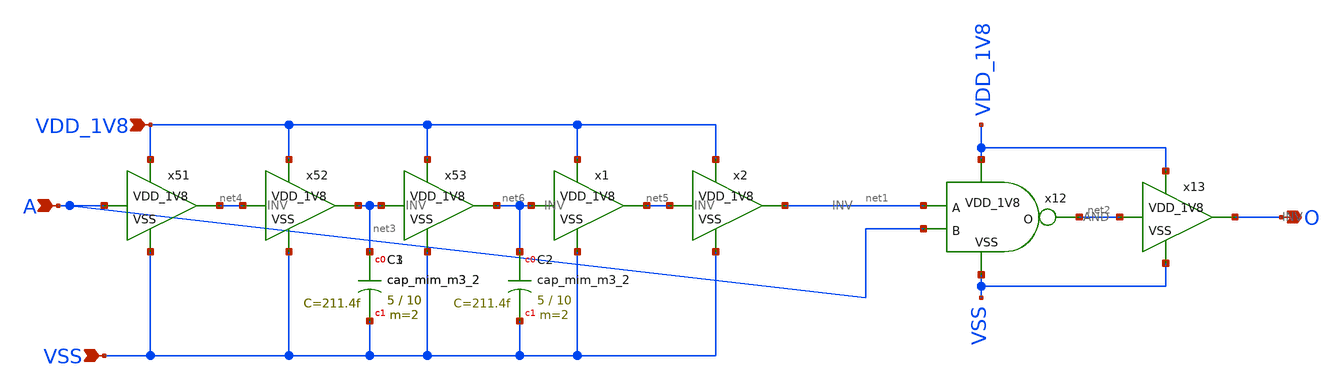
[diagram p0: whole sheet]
** sch_path: design/CNR_GR05_SKY130NM/POSEDGE.sch
**.subckt POSEDGE O VDD_1V8 VSS A
*.opin O
*.ipin VDD_1V8
*.ipin VSS
*.ipin A
x12 VDD_1V8 net1 A net2 VSS AND
x13 VDD_1V8 net2 O VSS INV
x51 VDD_1V8 A net4 VSS INV
x52 VDD_1V8 net4 net3 VSS INV
x53 VDD_1V8 net3 net6 VSS INV
x1 VDD_1V8 net6 net5 VSS INV
x2 VDD_1V8 net5 net1 VSS INV
XC3 net3 VSS sky130_fd_pr__cap_mim_m3_2 W=5 L=10 MF=2 m=2
XC1 net3 VSS sky130_fd_pr__cap_mim_m3_2 W=5 L=10 MF=2 m=2
XC2 net6 VSS sky130_fd_pr__cap_mim_m3_2 W=5 L=10 MF=2 m=2
**.ends
.end
